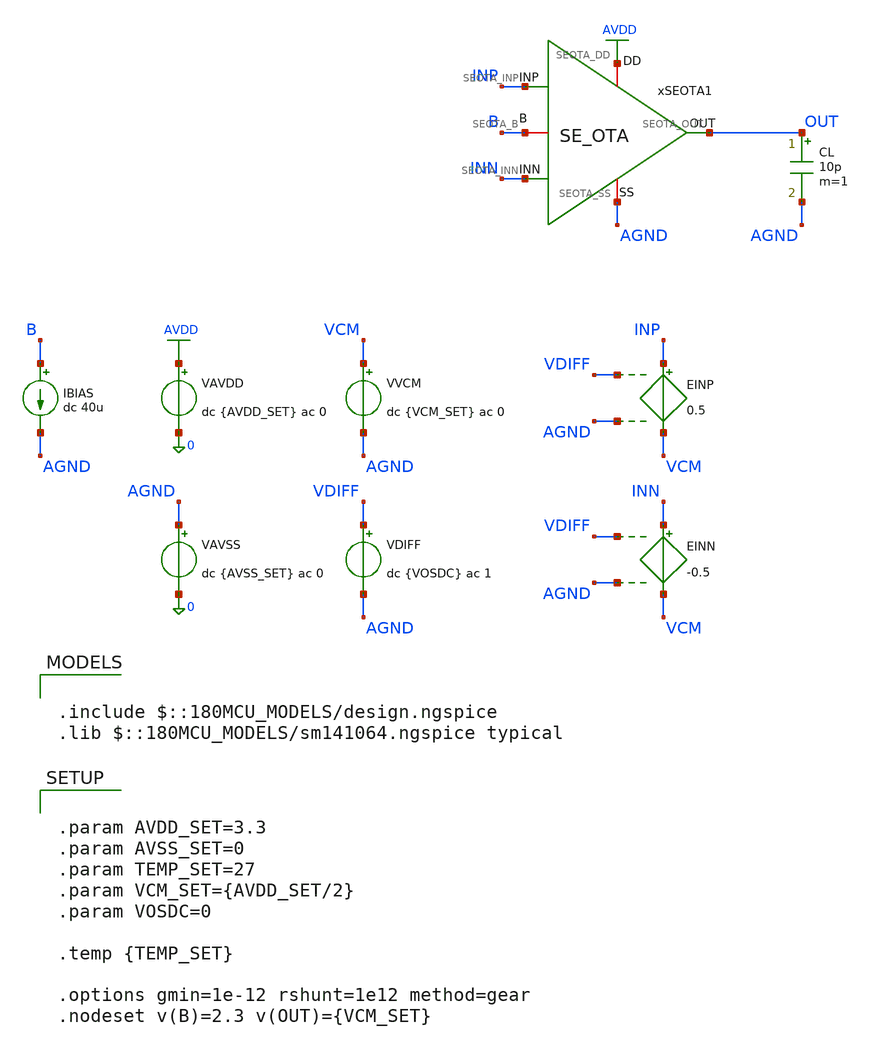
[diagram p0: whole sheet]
** sch_path: Design_Files/IC Design/Testbench/SE_OTA/Open_Loop/SE_OTA_TB_OL_NOM.sch
**.subckt SE_OTA_TB_OL_NOM
IBIAS B AGND dc 40u
VAVDD AVDD 0 dc {AVDD_SET} ac 0
.save i(vavdd)
CL OUT AGND 10p m=1
VVCM VCM AGND dc {VCM_SET} ac 0
VDIFF VDIFF AGND dc {VOSDC} ac 1
xSEOTA1 AVDD AGND INP INN OUT B SE_OTA
VAVSS AGND 0 dc {AVSS_SET} ac 0
.save i(vavss)
EINN INN VCM VDIFF AGND -0.5
EINP INP VCM VDIFF AGND 0.5
**** begin user architecture code

.include $::180MCU_MODELS/design.ngspice
.lib $::180MCU_MODELS/sm141064.ngspice typical



.control
destroy all
save all
set wr_vecnames
set wr_singlescale

shell mkdir -p
+ /foss/designs/ECG_Acquisition_IC/Measurement_Results/IC_Simulation/SE_OTA/NOM.Result_txt

shell rm -f
+ /foss/designs/ECG_Acquisition_IC/Measurement_Results/IC_Simulation/SE_OTA/NOM.Result_txt/NOM.op.txt
shell rm -f
+ /foss/designs/ECG_Acquisition_IC/Measurement_Results/IC_Simulation/SE_OTA/NOM.Result_txt/NOM.ol_vtc.txt
shell rm -f
+ /foss/designs/ECG_Acquisition_IC/Measurement_Results/IC_Simulation/SE_OTA/NOM.Result_txt/NOM.ol_ac.txt
shell rm -f
+ /foss/designs/ECG_Acquisition_IC/Measurement_Results/IC_Simulation/SE_OTA/NOM.Result_txt/NOM.ol_icmr.txt
shell rm -f
+ /foss/designs/ECG_Acquisition_IC/Measurement_Results/IC_Simulation/SE_OTA/NOM.Result_txt/NOM.cm_ac.txt
shell rm -f
+ /foss/designs/ECG_Acquisition_IC/Measurement_Results/IC_Simulation/SE_OTA/NOM.Result_txt/NOM.psrrp_ac.txt
shell rm -f
+ /foss/designs/ECG_Acquisition_IC/Measurement_Results/IC_Simulation/SE_OTA/NOM.Result_txt/NOM.psrrn_ac.txt

let avdd_run = 3.3
let vss_run  = 0
let vcm_run  = avdd_run/2

* set this from offset
let vos_run  = 0

* OP
alter @VVCM[DC] = $&vcm_run
alter @VDIFF[DC] = $&vos_run
alter @VVCM[ACMAG] = 0
alter @VDIFF[ACMAG] = 0
alter @VAVDD[ACMAG] = 0
alter @VAVSS[ACMAG] = 0

op

let op_vdd   = v(avdd) - v(agnd)
let op_vss   = v(agnd)
let op_vcm   = v(vcm) - v(agnd)
let op_vos   = v(vdiff) - v(agnd)
let op_vinp  = v(inp) - v(agnd)
let op_vinn  = v(inn) - v(agnd)
let op_vout  = v(out) - v(agnd)
let op_ibias = 40e-6
let op_idd   = -vavdd#branch
let op_iout  = 0

wrdata
+ /foss/designs/ECG_Acquisition_IC/Measurement_Results/IC_Simulation/SE_OTA/NOM.Result_txt/NOM.op.txt op_vdd op_vss op_vcm op_vos op_vinp op_vinn op_vout op_ibias op_idd op_iout

* OL VTC
alter @VVCM[DC] = $&vcm_run
alter @VDIFF[ACMAG] = 0

dc VDIFF -0.2 0.2 0.001

let vtc_vdiff = v(vdiff) - v(agnd)
let vtc_vinp  = v(inp) - v(agnd)
let vtc_vinn  = v(inn) - v(agnd)
let vtc_vout  = v(out) - v(agnd)
let vtc_ibias = 40e-6
let vtc_idd   = -vavdd#branch
let vtc_iout  = 0

wrdata
+ /foss/designs/ECG_Acquisition_IC/Measurement_Results/IC_Simulation/SE_OTA/NOM.Result_txt/NOM.ol_vtc.txt vtc_vdiff vtc_vinp vtc_vinn vtc_vout vtc_ibias vtc_idd vtc_iout

* OL AC
alter @VVCM[DC] = $&vcm_run
alter @VDIFF[DC] = $&vos_run
alter @VVCM[ACMAG] = 0
alter @VDIFF[ACMAG] = 1
alter @VDIFF[ACPHASE] = 0
alter @VAVDD[ACMAG] = 0
alter @VAVSS[ACMAG] = 0

ac dec 200 1 1G

let ol_out = v(out) - v(agnd)
let ad_real = real(ol_out)
let ad_imag = imag(ol_out)
let ad_mag  = mag(ol_out)
let ad_db   = db(ol_out)
let ad_ph   = ph(ol_out)

wrdata
+ /foss/designs/ECG_Acquisition_IC/Measurement_Results/IC_Simulation/SE_OTA/NOM.Result_txt/NOM.ol_ac.txt ad_real ad_imag ad_mag ad_db ad_ph

* ICMR DC
alter @VVCM[ACMAG] = 0
alter @VDIFF[ACMAG] = 0
alter @VAVDD[ACMAG] = 0
alter @VAVSS[ACMAG] = 0

dc VVCM 0 $&avdd_run 0.01 VDIFF -0.2 0.2 0.001

let icmr_vcm   = v(vcm) - v(agnd)
let icmr_vdiff = v(vdiff) - v(agnd)
let icmr_vout  = v(out) - v(agnd)
let icmr_ibias = 40e-6
let icmr_idd   = -vavdd#branch
let icmr_iout  = 0

wrdata
+ /foss/designs/ECG_Acquisition_IC/Measurement_Results/IC_Simulation/SE_OTA/NOM.Result_txt/NOM.ol_icmr.txt icmr_vcm icmr_vdiff icmr_vout icmr_ibias icmr_idd icmr_iout

* CM AC
alter @VVCM[DC] = $&vcm_run
alter @VDIFF[DC] = $&vos_run
alter @VVCM[ACMAG] = 1
alter @VVCM[ACPHASE] = 0
alter @VDIFF[ACMAG] = 0
alter @VAVDD[ACMAG] = 0
alter @VAVSS[ACMAG] = 0

ac dec 200 1 1G

let cm_out  = v(out) - v(agnd)
let acm_real = real(cm_out)
let acm_imag = imag(cm_out)

wrdata
+ /foss/designs/ECG_Acquisition_IC/Measurement_Results/IC_Simulation/SE_OTA/NOM.Result_txt/NOM.cm_ac.txt acm_real acm_imag

* PSRR+
alter @VVCM[ACMAG] = 0
alter @VDIFF[ACMAG] = 0
alter @VAVDD[ACMAG] = 1
alter @VAVDD[ACPHASE] = 0
alter @VAVSS[ACMAG] = 0

ac dec 200 1 1G

let psrrp_out  = v(out) - v(agnd)
let psrrp_real = real(psrrp_out)
let psrrp_imag = imag(psrrp_out)

wrdata
+ /foss/designs/ECG_Acquisition_IC/Measurement_Results/IC_Simulation/SE_OTA/NOM.Result_txt/NOM.psrrp_ac.txt psrrp_real psrrp_imag

* PSRR-
alter @VVCM[ACMAG] = 0
alter @VDIFF[ACMAG] = 0
alter @VAVDD[ACMAG] = 0
alter @VAVSS[ACMAG] = 1
alter @VAVSS[ACPHASE] = 0

ac dec 200 1 1G

let psrrn_out  = v(out) - v(agnd)
let psrrn_real = real(psrrn_out)
let psrrn_imag = imag(psrrn_out)

wrdata
+ /foss/designs/ECG_Acquisition_IC/Measurement_Results/IC_Simulation/SE_OTA/NOM.Result_txt/NOM.psrrn_ac.txt psrrn_real psrrn_imag

.endc




.param AVDD_SET=3.3
.param AVSS_SET=0
.param TEMP_SET=27
.param VCM_SET={AVDD_SET/2}
.param VOSDC=0

.temp {TEMP_SET}

.options gmin=1e-12 rshunt=1e12 method=gear
.nodeset v(B)=2.3 v(OUT)={VCM_SET}


**** end user architecture code
**.ends

* expanding   symbol:  ECG_Acquisition_IC/Design_Files/IC Design/Schematic/SE_OTA/SE_OTA.sym # of
*+ pins=6
** sym_path: Design_Files/IC Design/Schematic/SE_OTA/SE_OTA.sym
** sch_path: Design_Files/IC Design/Schematic/SE_OTA/SE_OTA.sch
.subckt SE_OTA SEOTA_DD SEOTA_SS SEOTA_INP SEOTA_INN SEOTA_OUT SEOTA_B
*.iopin SEOTA_DD
*.iopin SEOTA_SS
*.ipin SEOTA_INP
*.ipin SEOTA_INN
*.opin SEOTA_OUT
*.iopin SEOTA_B
XM3 net4 net4 SEOTA_DD SEOTA_DD pfet_03v3 L=4u W=1u nf=1 ad='int((nf+1)/2) * W/nf * 0.18u' as='int((nf+2)/2) * W/nf * 0.18u'
+ pd='2*int((nf+1)/2) * (W/nf + 0.18u)' ps='2*int((nf+2)/2) * (W/nf + 0.18u)' nrd='0.18u / W' nrs='0.18u / W'
+ sa=0 sb=0 sd=0 m=60
XM7 SEOTA_OUT SEOTA_B SEOTA_SS SEOTA_SS nfet_03v3 L=0.5u W=1u nf=1 ad='int((nf+1)/2) * W/nf * 0.18u'
+ as='int((nf+2)/2) * W/nf * 0.18u' pd='2*int((nf+1)/2) * (W/nf + 0.18u)' ps='2*int((nf+2)/2) * (W/nf + 0.18u)'
+ nrd='0.18u / W' nrs='0.18u / W' sa=0 sb=0 sd=0 m=100
Rz net1 net2 3.8k m=1
XM5 net3 SEOTA_B SEOTA_SS SEOTA_SS nfet_03v3 L=2u W=1u nf=1 ad='int((nf+1)/2) * W/nf * 0.18u' as='int((nf+2)/2) * W/nf * 0.18u'
+ pd='2*int((nf+1)/2) * (W/nf + 0.18u)' ps='2*int((nf+2)/2) * (W/nf + 0.18u)' nrd='0.18u / W' nrs='0.18u / W'
+ sa=0 sb=0 sd=0 m=10
XM6 SEOTA_OUT net1 SEOTA_DD SEOTA_DD pfet_03v3 L=0.5u W=1u nf=1 ad='int((nf+1)/2) * W/nf * 0.18u' as='int((nf+2)/2) * W/nf * 0.18u'
+ pd='2*int((nf+1)/2) * (W/nf + 0.18u)' ps='2*int((nf+2)/2) * (W/nf + 0.18u)' nrd='0.18u / W' nrs='0.18u / W'
+ sa=0 sb=0 sd=0 m=400
XM8 SEOTA_B SEOTA_B SEOTA_SS SEOTA_SS nfet_03v3 L=2u W=1u nf=1 ad='int((nf+1)/2) * W/nf * 0.18u' as='int((nf+2)/2) * W/nf * 0.18u'
+ pd='2*int((nf+1)/2) * (W/nf + 0.18u)' ps='2*int((nf+2)/2) * (W/nf + 0.18u)' nrd='0.18u / W' nrs='0.18u / W'
+ sa=0 sb=0 sd=0 m=20
Cc net2 SEOTA_OUT 2p m=1
XM4 net1 net4 SEOTA_DD SEOTA_DD pfet_03v3 L=4u W=1u nf=1 ad='int((nf+1)/2) * W/nf * 0.18u' as='int((nf+2)/2) * W/nf * 0.18u'
+ pd='2*int((nf+1)/2) * (W/nf + 0.18u)' ps='2*int((nf+2)/2) * (W/nf + 0.18u)' nrd='0.18u / W' nrs='0.18u / W'
+ sa=0 sb=0 sd=0 m=60
XM1 net4 SEOTA_INN net3 SEOTA_SS nfet_03v3 L=4u W=1u nf=1 ad='int((nf+1)/2) * W/nf * 0.18u' as='int((nf+2)/2) * W/nf * 0.18u'
+ pd='2*int((nf+1)/2) * (W/nf + 0.18u)' ps='2*int((nf+2)/2) * (W/nf + 0.18u)' nrd='0.18u / W' nrs='0.18u / W'
+ sa=0 sb=0 sd=0 m=400
XM2 net1 SEOTA_INP net3 SEOTA_SS nfet_03v3 L=4u W=1u nf=1 ad='int((nf+1)/2) * W/nf * 0.18u' as='int((nf+2)/2) * W/nf * 0.18u'
+ pd='2*int((nf+1)/2) * (W/nf + 0.18u)' ps='2*int((nf+2)/2) * (W/nf + 0.18u)' nrd='0.18u / W' nrs='0.18u / W'
+ sa=0 sb=0 sd=0 m=400
.ends

.GLOBAL AVDD
.end
